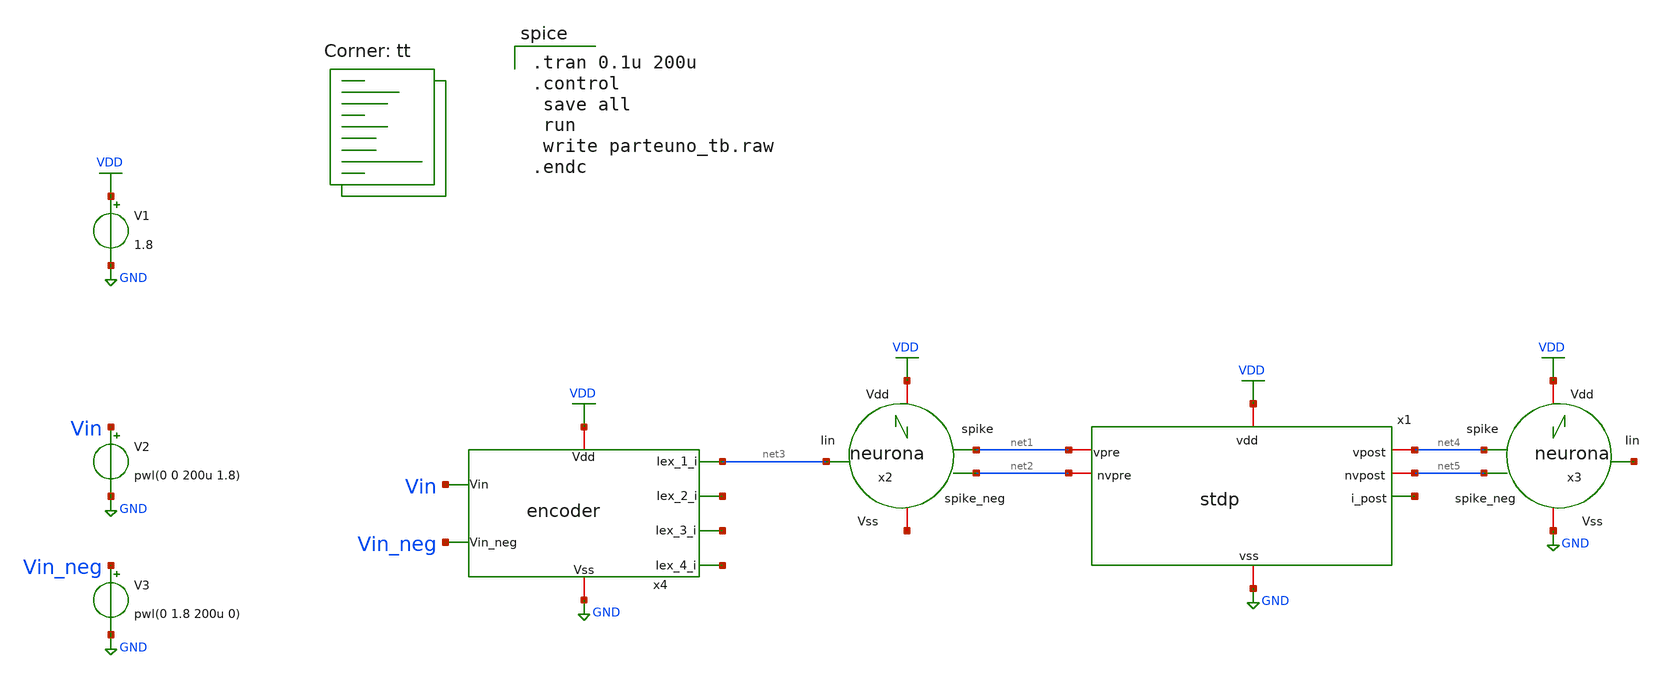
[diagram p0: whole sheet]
** sch_path: designs/libs/snn_analog/stdp/sch/untitled.sch
**.subckt untitled
x1 VDD GND net6 net1 net2 net5 net4 stdp
x2 net3 VDD net7 net1 net2 neurona
x3 net8 VDD GND net4 net5 neurona
x4 VDD GND Vin Vin_neg net3 net9 net10 net11 encoder
V1 VDD GND 1.8
V2 Vin GND pwl(0 0 200u 1.8)
V3 Vin_neg GND pwl(0 1.8 200u 0)
**** begin user architecture code
.lib $::SKYWATER_MODELS/sky130.lib.spice tt

.tran 0.1u 200u
.control
 save all
 run
 write parteuno_tb.raw
.endc

**** end user architecture code
**.ends
.GLOBAL GND
.GLOBAL VDD
.end
